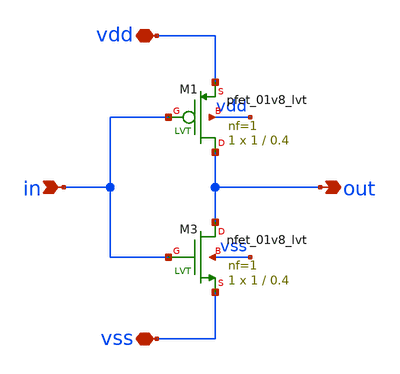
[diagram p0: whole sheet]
** sch_path: post_layout/sar/latch/logic/inv_lvt.sch
**.subckt inv_lvt vdd vss in out
*.iopin vdd
*.iopin vss
*.ipin in
*.opin out
XM3 out in vss vss sky130_fd_pr__nfet_01v8_lvt L=0.4 W=1 nf=1 ad='int((nf+1)/2) * W/nf * 0.29' as='int((nf+2)/2) * W/nf * 0.29'
+ pd='2*int((nf+1)/2) * (W/nf + 0.29)' ps='2*int((nf+2)/2) * (W/nf + 0.29)' nrd='0.29 / W' nrs='0.29 / W'
+ sa=0 sb=0 sd=0 mult=1 m=1
XM1 out in vdd vdd sky130_fd_pr__pfet_01v8_lvt L=0.4 W=1 nf=1 ad='int((nf+1)/2) * W/nf * 0.29' as='int((nf+2)/2) * W/nf * 0.29'
+ pd='2*int((nf+1)/2) * (W/nf + 0.29)' ps='2*int((nf+2)/2) * (W/nf + 0.29)' nrd='0.29 / W' nrs='0.29 / W'
+ sa=0 sb=0 sd=0 mult=1 m=1
**.ends
.end
